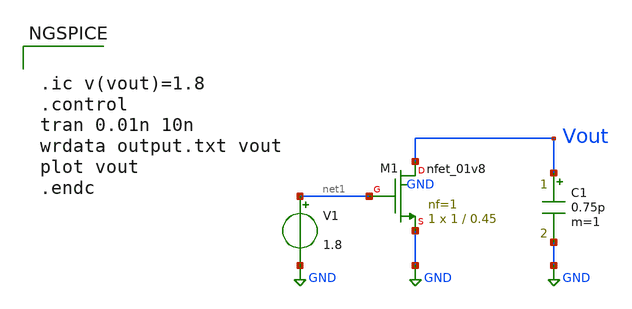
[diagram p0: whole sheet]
** sch_path: Circuiti/transitorio_carica.sch
**.subckt transitorio_carica
XM1 Vout net1 GND GND sky130_fd_pr__nfet_01v8 L=0.45 W=1 nf=1 ad='int((nf+1)/2) * W/nf * 0.29' as='int((nf+2)/2) * W/nf * 0.29'
+ pd='2*int((nf+1)/2) * (W/nf + 0.29)' ps='2*int((nf+2)/2) * (W/nf + 0.29)' nrd='0.29 / W' nrs='0.29 / W'
+ sa=0 sb=0 sd=0 mult=1 m=1
V1 net1 GND 1.8
C1 Vout GND 0.75p m=1
**** begin user architecture code


.lib /home/matteo/xschem_downloads/skywater-pdk/libraries/sky130_fd_pr_ngspice/latest/models/sky130.lib.spice ss

*.include /home/matteo/xschem_downloads/skywater-pdk/libraries/sky130_fd_pr_ngspice/latest/cells/nfet_01v8/sky130_fd_pr__nfet_01v8__tt.corner.spice

.param mc_mm_switch=0
.param mc_pr_switch=1




.ic v(vout)=1.8
.control
tran 0.01n 10n
wrdata output.txt vout
plot vout
.endc


**** end user architecture code
**.ends
.GLOBAL GND
.end
